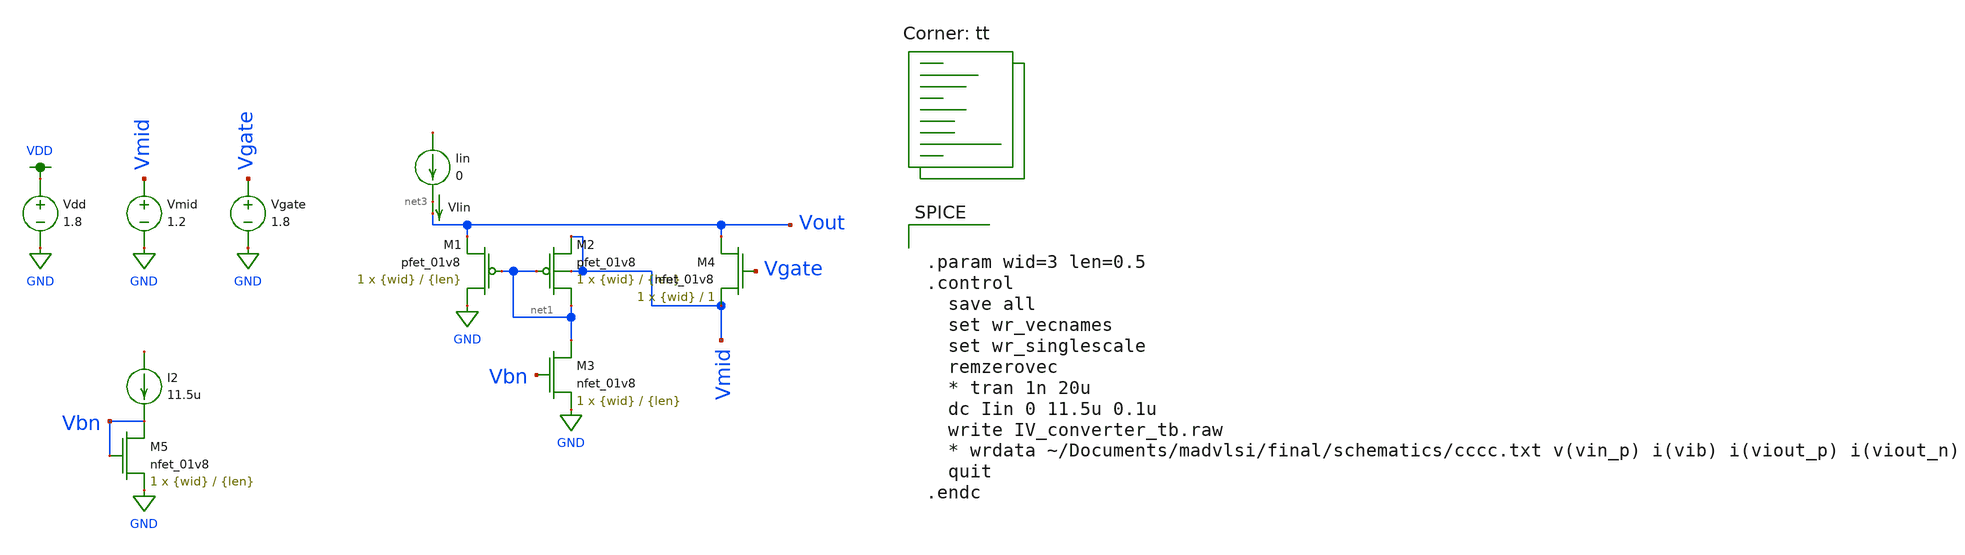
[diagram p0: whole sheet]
** sch_path: final/schematics/IV_converter_tb.sch
**.subckt IV_converter_tb
XM1 GND net1 Vout VDD sky130_fd_pr__pfet_01v8 L={len} W={wid} nf=1 ad='int((nf+1)/2) * W/nf * 0.29' as='int((nf+2)/2) * W/nf * 0.29'
+ pd='2*int((nf+1)/2) * (W/nf + 0.29)' ps='2*int((nf+2)/2) * (W/nf + 0.29)' nrd='0.29 / W' nrs='0.29 / W'
+ sa=0 sb=0 sd=0 mult=1 m=1
XM2 net1 net1 Vmid Vmid sky130_fd_pr__pfet_01v8 L={len} W={wid} nf=1 ad='int((nf+1)/2) * W/nf * 0.29'
+ as='int((nf+2)/2) * W/nf * 0.29' pd='2*int((nf+1)/2) * (W/nf + 0.29)' ps='2*int((nf+2)/2) * (W/nf + 0.29)'
+ nrd='0.29 / W' nrs='0.29 / W' sa=0 sb=0 sd=0 mult=1 m=1
Vdd VDD GND 1.8
Iin net2 net3 0
I2 net4 Vbn 11.5u
XM5 Vbn Vbn GND GND sky130_fd_pr__nfet_01v8 L={len} W={wid} nf=1 ad='int((nf+1)/2) * W/nf * 0.29' as='int((nf+2)/2) * W/nf * 0.29'
+ pd='2*int((nf+1)/2) * (W/nf + 0.29)' ps='2*int((nf+2)/2) * (W/nf + 0.29)' nrd='0.29 / W' nrs='0.29 / W'
+ sa=0 sb=0 sd=0 mult=1 m=1
Vmid Vmid GND 1.2
Vgate Vgate GND 1.8
XM3 net1 Vbn GND GND sky130_fd_pr__nfet_01v8 L={len} W={wid} nf=1 ad='int((nf+1)/2) * W/nf * 0.29' as='int((nf+2)/2) * W/nf * 0.29'
+ pd='2*int((nf+1)/2) * (W/nf + 0.29)' ps='2*int((nf+2)/2) * (W/nf + 0.29)' nrd='0.29 / W' nrs='0.29 / W'
+ sa=0 sb=0 sd=0 mult=1 m=1
XM4 Vout Vgate Vmid GND sky130_fd_pr__nfet_01v8 L=1 W={wid} nf=1 ad='int((nf+1)/2) * W/nf * 0.29' as='int((nf+2)/2) * W/nf * 0.29'
+ pd='2*int((nf+1)/2) * (W/nf + 0.29)' ps='2*int((nf+2)/2) * (W/nf + 0.29)' nrd='0.29 / W' nrs='0.29 / W'
+ sa=0 sb=0 sd=0 mult=1 m=1
VIin net3 Vout 0
.save i(viin)
**** begin user architecture code


.param wid=3 len=0.5
.control
  save all
  set wr_vecnames
  set wr_singlescale
  remzerovec
  * tran 1n 20u
  dc Iin 0 11.5u 0.1u
  write IV_converter_tb.raw
  * wrdata ~/Documents/madvlsi/final/schematics/cccc.txt v(vin_p) i(vib) i(viout_p) i(viout_n)
  quit
.endc


.lib $::SKYWATER_MODELS/sky130.lib.spice tt
**** end user architecture code
**.ends
.GLOBAL GND
.GLOBAL VDD
.end
